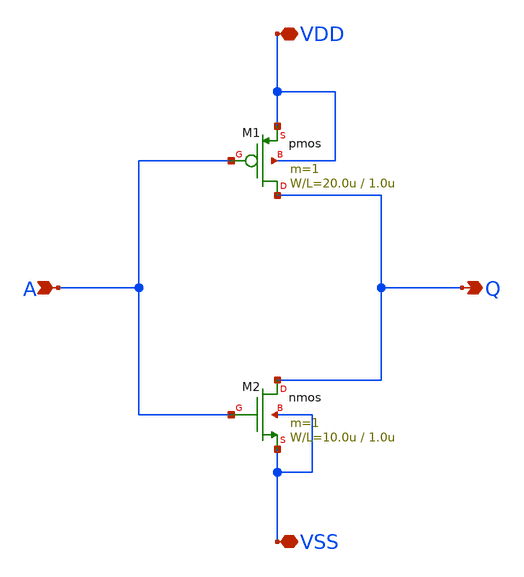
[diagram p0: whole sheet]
** sch_path: member_project/sanken/iijima/inverter/iijima_inverter.sch
**.subckt iijima_inverter A Q VDD VSS
*.ipin A
*.opin Q
*.iopin VDD
*.iopin VSS
M1 Q A VDD VDD pmos L=1.0u W=20.0u m=1
M2 Q A VSS VSS nmos L=1.0u W=10.0u m=1
**.ends
.end
